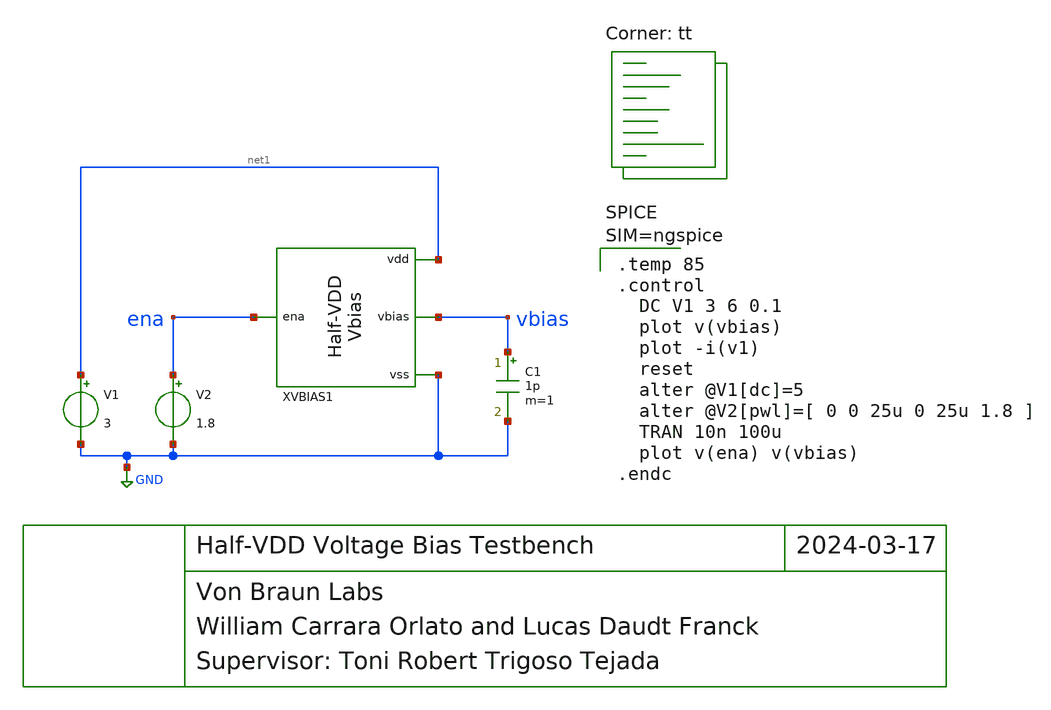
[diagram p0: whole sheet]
** sch_path: xschem_final/halfvdd_vbias_tb.sch
**.subckt halfvdd_vbias_tb
XVBIAS1 net1 vbias ena GND halfvdd_vbias
V1 net1 GND 3
V2 ena GND 1.8
C1 vbias GND 1p m=1
**** begin user architecture code
.lib $::SKYWATER_MODELS/sky130.lib.spice tt


.temp 85
.control
  DC V1 3 6 0.1
  plot v(vbias)
  plot -i(v1)
  reset
  alter @V1[dc]=5
  alter @V2[pwl]=[ 0 0 25u 0 25u 1.8 ]
  TRAN 10n 100u
  plot v(ena) v(vbias)
.endc



**** end user architecture code
**.ends

* expanding   symbol:  halfvdd_vbias.sym # of pins=4
** sym_path: xschem_final/halfvdd_vbias.sym
** sch_path: xschem_final/halfvdd_vbias.sch
.subckt halfvdd_vbias vdd vbias ena vss
*.ipin ena
*.iopin vss
*.iopin vdd
*.opin vbias
XM1 net3 net3 vdd vdd sky130_fd_pr__pfet_g5v0d10v5 L=5 W=1 nf=1 ad='int((nf+1)/2) * W/nf * 0.29' as='int((nf+2)/2) * W/nf * 0.29'
+ pd='2*int((nf+1)/2) * (W/nf + 0.29)' ps='2*int((nf+2)/2) * (W/nf + 0.29)' nrd='0.29 / W' nrs='0.29 / W'
+ sa=0 sb=0 sd=0 mult=1 m=1
XM2 net3 net3 vbias vbias sky130_fd_pr__pfet_g5v0d10v5 L=5 W=1 nf=1 ad='int((nf+1)/2) * W/nf * 0.29'
+ as='int((nf+2)/2) * W/nf * 0.29' pd='2*int((nf+1)/2) * (W/nf + 0.29)' ps='2*int((nf+2)/2) * (W/nf + 0.29)'
+ nrd='0.29 / W' nrs='0.29 / W' sa=0 sb=0 sd=0 mult=1 m=1
XM3 net2 net2 vbias vbias sky130_fd_pr__pfet_g5v0d10v5 L=5 W=1 nf=1 ad='int((nf+1)/2) * W/nf * 0.29'
+ as='int((nf+2)/2) * W/nf * 0.29' pd='2*int((nf+1)/2) * (W/nf + 0.29)' ps='2*int((nf+2)/2) * (W/nf + 0.29)'
+ nrd='0.29 / W' nrs='0.29 / W' sa=0 sb=0 sd=0 mult=1 m=1
XM4 net2 net2 net1 net1 sky130_fd_pr__pfet_g5v0d10v5 L=5 W=1 nf=1 ad='int((nf+1)/2) * W/nf * 0.29' as='int((nf+2)/2) * W/nf * 0.29'
+ pd='2*int((nf+1)/2) * (W/nf + 0.29)' ps='2*int((nf+2)/2) * (W/nf + 0.29)' nrd='0.29 / W' nrs='0.29 / W'
+ sa=0 sb=0 sd=0 mult=1 m=1
XM5 net1 ena vss vss sky130_fd_pr__nfet_g5v0d10v5 L=1 W=5 nf=1 ad='int((nf+1)/2) * W/nf * 0.29' as='int((nf+2)/2) * W/nf * 0.29'
+ pd='2*int((nf+1)/2) * (W/nf + 0.29)' ps='2*int((nf+2)/2) * (W/nf + 0.29)' nrd='0.29 / W' nrs='0.29 / W'
+ sa=0 sb=0 sd=0 mult=1 m=1
.ends

.GLOBAL GND
.end
